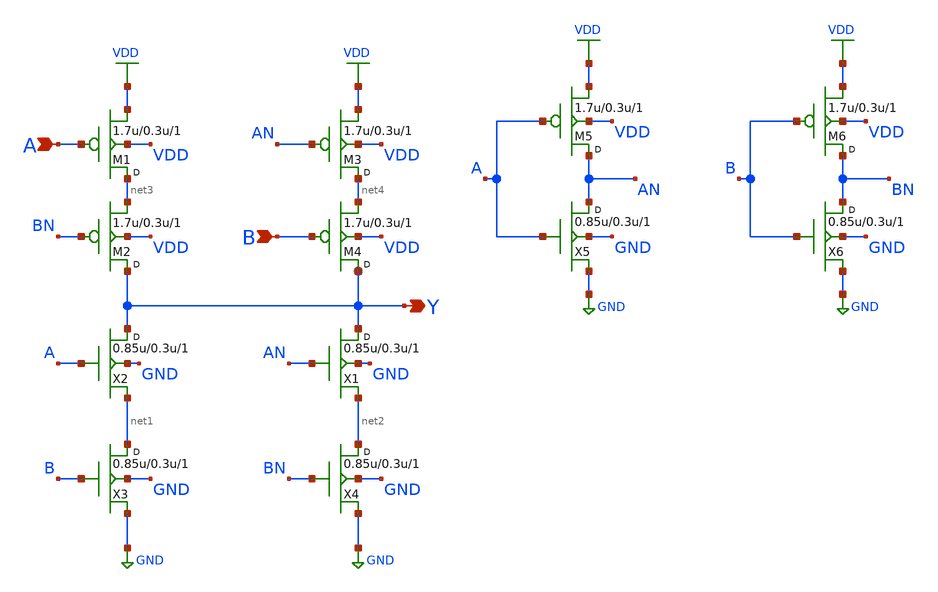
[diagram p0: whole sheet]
** sch_path: openfasoc/common/platforms/gf180mcuosu9Txor21/gf180mcu_osu_sc_xor2_1.sch
**.subckt gf180mcu_osu_sc_xor2_1 B A Y
*.ipin B
*.ipin A
*.opin Y
X2 Y A net1 GND nmos_3p3 w=0.85u l=0.3u m=1
X3 net1 B GND GND nmos_3p3 w=0.85u l=0.3u m=1
X1 Y AN net2 GND nmos_3p3 w=0.85u l=0.3u m=1
X4 net2 BN GND GND nmos_3p3 w=0.85u l=0.3u m=1
M1 net3 A VDD VDD pmos_3p3 w=1.7u l=0.3u m=1
M2 Y BN net3 VDD pmos_3p3 w=1.7u l=0.3u m=1
M3 net4 AN VDD VDD pmos_3p3 w=1.7u l=0.3u m=1
M4 Y B net4 VDD pmos_3p3 w=1.7u l=0.3u m=1
X5 AN A GND GND nmos_3p3 w=0.85u l=0.3u m=1
M5 AN A VDD VDD pmos_3p3 w=1.7u l=0.3u m=1
X6 BN B GND GND nmos_3p3 w=0.85u l=0.3u m=1
M6 BN B VDD VDD pmos_3p3 w=1.7u l=0.3u m=1
**.ends
.GLOBAL GND
.GLOBAL VDD
.end
